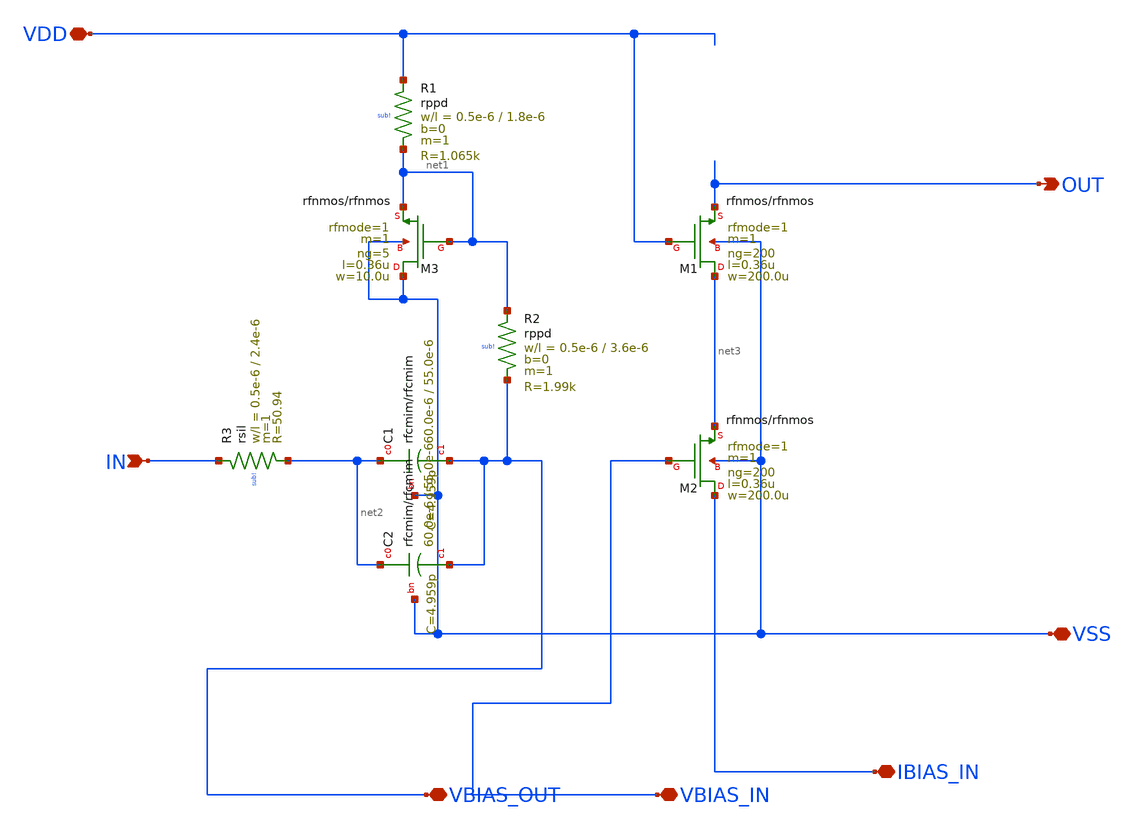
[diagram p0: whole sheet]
** sch_path: GPS_LNA/design_data/xschem/lna_nmos_base.sch
**.subckt lna_nmos_base VDD IN OUT VSS VBIAS_IN VBIAS_OUT IBIAS_IN
*.iopin VDD
*.ipin IN
*.opin OUT
*.iopin VSS
*.iopin VBIAS_IN
*.iopin VBIAS_OUT
*.iopin IBIAS_IN
XR2 net1 VBIAS_OUT sub! rppd w=0.5e-6 l=3.6e-6 m=1 b=0 mm_ok=1
XR1 VDD net1 sub! rppd w=0.5e-6 l=1.8e-6 m=1 b=0 mm_ok=1
XR3 IN net2 sub! rsil w=0.5e-6 l=2.4e-6 m=1 mm_ok=1
XC1 net2 VBIAS_OUT VSS rfcmim w=60.0e-6 l=55.0e-6 wfeed=5.0e-6 m=1 mm_ok=1
XC2 net2 VBIAS_OUT VSS rfcmim w=60.0e-6 l=55.0e-6 wfeed=5.0e-6 m=1 mm_ok=1
XM3 VSS net1 net1 VSS rfnmos w=10.0u l=0.36u ng=5 m=1 rfmode=1 mm_ok=1
XM2 IBIAS_IN VBIAS_IN net3 VSS rfnmos w=200.0u l=0.36u ng=200 m=1 rfmode=1 mm_ok=1
XM1 net3 VDD OUT VSS rfnmos w=200.0u l=0.36u ng=200 m=1 rfmode=1 mm_ok=1
**.ends
.end
